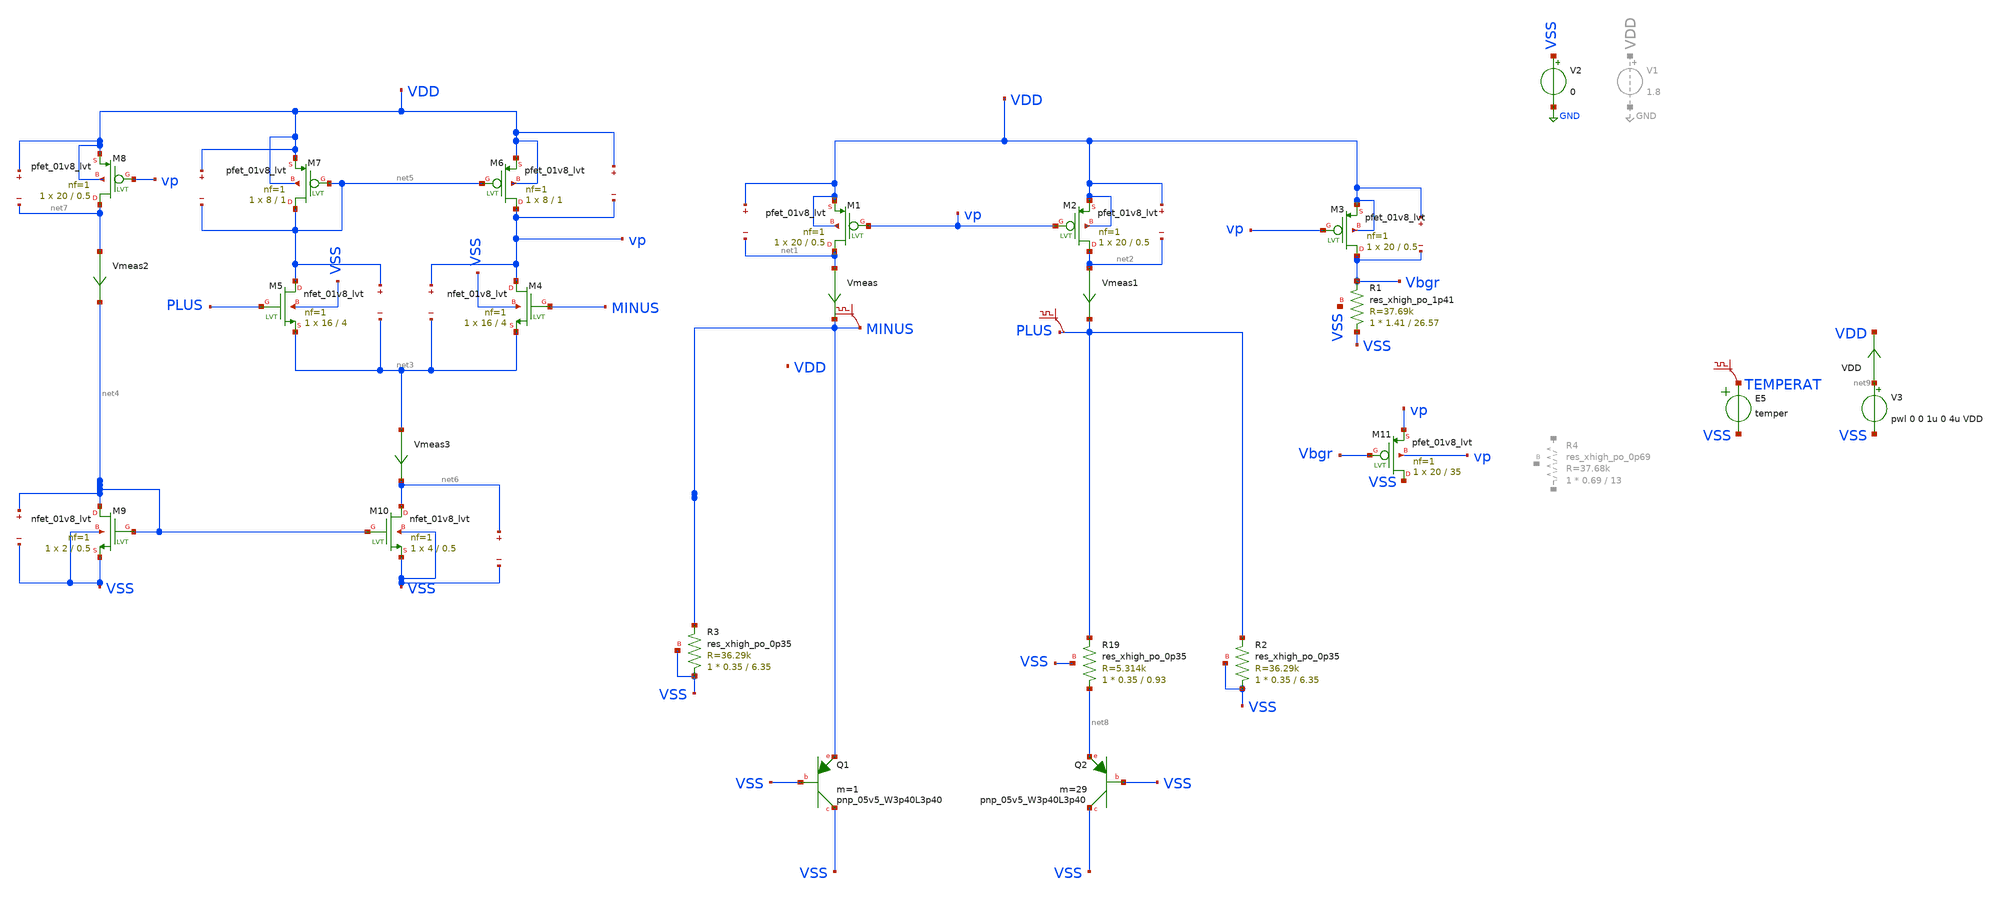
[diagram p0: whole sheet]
** sch_path: xschem/BGRwOpampRes.sch
**.subckt BGRwOpampRes
XQ1 VSS VSS MINUS sky130_fd_pr__pnp_05v5_W3p40L3p40 m=1
XQ2 VSS VSS net8 sky130_fd_pr__pnp_05v5_W3p40L3p40 m=29
XM1 net1 vp VDD VDD sky130_fd_pr__pfet_01v8_lvt L=0.5 W=20 nf=1 ad='int((nf+1)/2) * W/nf * 0.29' as='int((nf+2)/2) * W/nf * 0.29'
+ pd='2*int((nf+1)/2) * (W/nf + 0.29)' ps='2*int((nf+2)/2) * (W/nf + 0.29)' nrd='0.29 / W' nrs='0.29 / W'
+ sa=0 sb=0 sd=0 mult=1 m=1
XM2 net2 vp VDD VDD sky130_fd_pr__pfet_01v8_lvt L=0.5 W=20 nf=1 ad='int((nf+1)/2) * W/nf * 0.29' as='int((nf+2)/2) * W/nf * 0.29'
+ pd='2*int((nf+1)/2) * (W/nf + 0.29)' ps='2*int((nf+2)/2) * (W/nf + 0.29)' nrd='0.29 / W' nrs='0.29 / W'
+ sa=0 sb=0 sd=0 mult=1 m=1
XM3 Vbgr vp VDD VDD sky130_fd_pr__pfet_01v8_lvt L=0.5 W=20 nf=1 ad='int((nf+1)/2) * W/nf * 0.29' as='int((nf+2)/2) * W/nf * 0.29'
+ pd='2*int((nf+1)/2) * (W/nf + 0.29)' ps='2*int((nf+2)/2) * (W/nf + 0.29)' nrd='0.29 / W' nrs='0.29 / W'
+ sa=0 sb=0 sd=0 mult=1 m=1
V2 VSS GND 0
Vmeas net1 MINUS 0
.save i(vmeas)
Vmeas1 net2 PLUS 0
.save i(vmeas1)
.save v(vdd)
.save v(net1)
.save v(vdd)
.save v(net2)
.save v(vdd)
.save v(vbgr)
XM4 vp MINUS net3 VSS sky130_fd_pr__nfet_01v8_lvt L=4 W=16 nf=1 ad='int((nf+1)/2) * W/nf * 0.29' as='int((nf+2)/2) * W/nf * 0.29'
+ pd='2*int((nf+1)/2) * (W/nf + 0.29)' ps='2*int((nf+2)/2) * (W/nf + 0.29)' nrd='0.29 / W' nrs='0.29 / W'
+ sa=0 sb=0 sd=0 mult=1 m=1
XM5 net5 PLUS net3 VSS sky130_fd_pr__nfet_01v8_lvt L=4 W=16 nf=1 ad='int((nf+1)/2) * W/nf * 0.29' as='int((nf+2)/2) * W/nf * 0.29'
+ pd='2*int((nf+1)/2) * (W/nf + 0.29)' ps='2*int((nf+2)/2) * (W/nf + 0.29)' nrd='0.29 / W' nrs='0.29 / W'
+ sa=0 sb=0 sd=0 mult=1 m=1
XM6 vp net5 VDD VDD sky130_fd_pr__pfet_01v8_lvt L=1 W=8 nf=1 ad='int((nf+1)/2) * W/nf * 0.29' as='int((nf+2)/2) * W/nf * 0.29'
+ pd='2*int((nf+1)/2) * (W/nf + 0.29)' ps='2*int((nf+2)/2) * (W/nf + 0.29)' nrd='0.29 / W' nrs='0.29 / W'
+ sa=0 sb=0 sd=0 mult=1 m=1
.save v(vp)
.save v(net3)
.save v(net5)
.save v(net3)
XM10 net6 net4 VSS VSS sky130_fd_pr__nfet_01v8_lvt L=0.5 W=4 nf=1 ad='int((nf+1)/2) * W/nf * 0.29' as='int((nf+2)/2) * W/nf * 0.29'
+ pd='2*int((nf+1)/2) * (W/nf + 0.29)' ps='2*int((nf+2)/2) * (W/nf + 0.29)' nrd='0.29 / W' nrs='0.29 / W'
+ sa=0 sb=0 sd=0 mult=1 m=1
XM9 net4 net4 VSS VSS sky130_fd_pr__nfet_01v8_lvt L=0.5 W=2 nf=1 ad='int((nf+1)/2) * W/nf * 0.29' as='int((nf+2)/2) * W/nf * 0.29'
+ pd='2*int((nf+1)/2) * (W/nf + 0.29)' ps='2*int((nf+2)/2) * (W/nf + 0.29)' nrd='0.29 / W' nrs='0.29 / W'
+ sa=0 sb=0 sd=0 mult=1 m=1
XM7 net5 net5 VDD VDD sky130_fd_pr__pfet_01v8_lvt L=1 W=8 nf=1 ad='int((nf+1)/2) * W/nf * 0.29' as='int((nf+2)/2) * W/nf * 0.29'
+ pd='2*int((nf+1)/2) * (W/nf + 0.29)' ps='2*int((nf+2)/2) * (W/nf + 0.29)' nrd='0.29 / W' nrs='0.29 / W'
+ sa=0 sb=0 sd=0 mult=1 m=1
.save v(vdd)
.save v(net5)
.save v(vdd)
.save v(vp)
.save v(net6)
.save v(vss)
.save v(net4)
.save v(vss)
Vmeas3 net3 net6 0
.save i(vmeas3)
XM8 net7 vp VDD VDD sky130_fd_pr__pfet_01v8_lvt L=0.5 W=20 nf=1 ad='int((nf+1)/2) * W/nf * 0.29' as='int((nf+2)/2) * W/nf * 0.29'
+ pd='2*int((nf+1)/2) * (W/nf + 0.29)' ps='2*int((nf+2)/2) * (W/nf + 0.29)' nrd='0.29 / W' nrs='0.29 / W'
+ sa=0 sb=0 sd=0 mult=1 m=1
Vmeas2 net7 net4 0
.save i(vmeas2)
.save v(vdd)
.save v(net7)
XM11 VSS Vbgr vp vp sky130_fd_pr__pfet_01v8_lvt L=35 W=20 nf=1 ad='int((nf+1)/2) * W/nf * 0.29' as='int((nf+2)/2) * W/nf * 0.29'
+ pd='2*int((nf+1)/2) * (W/nf + 0.29)' ps='2*int((nf+2)/2) * (W/nf + 0.29)' nrd='0.29 / W' nrs='0.29 / W'
+ sa=0 sb=0 sd=0 mult=1 m=1
V3 net9 VSS pwl 0 0 1u 0 4u VDD
E5 TEMPERAT VSS VOL=' temper '
.save v(temperat)
VDD net9 VDD 0
.save i(vdd)
.save v(minus)
.save v(plus)
XR19 net8 PLUS VSS sky130_fd_pr__res_xhigh_po_0p35 L=0.93 mult=1 m=1
XR2 VSS PLUS VSS sky130_fd_pr__res_xhigh_po_0p35 L=6.35 mult=1 m=1
XR3 VSS MINUS VSS sky130_fd_pr__res_xhigh_po_0p35 L=6.35 mult=1 m=1
XR1 VSS Vbgr VSS sky130_fd_pr__res_xhigh_po_1p41 L=26.57 mult=1 m=1
**** begin user architecture code

** opencircuitdesign pdks install
.lib $::SKYWATER_MODELS/sky130.lib.spice tt




* this experimental option enables mos model bin
* selection based on W/NF instead of W
* .options wnflag=1 XMU=0.49 METHOD=GEAR ITL4=100 CHGTOL=1e-15 TRTOL=1 RELTOL=0.0001 VNTOL=0.1u
.param ABSVAR=0.03
.param VCCGAUSS=agauss(1.8, 'ABSVAR', 1)
.param VDD=VCCGAUSS
*.param VDD=1.8
** variation marameters:
* .options savecurrents
.control
  setseed 12
  reset
  let run=1
  dowhile run <= 100
    if run > 1
      reset
      set appendwrite
    end
    * save all
    if run % 3 = 1
      set temp=-40
    end
    if run % 3 = 2
      set temp=27
    end
    if run % 3 = 0
      set temp=125
    end
    echo "Run=$&run, Temp=$temp"
    tran 0.2u 50u
    write asal_tb_bandgap_r.raw
    let run = run + 1
  end
.endc


**** end user architecture code
**.ends
.GLOBAL GND
.end
